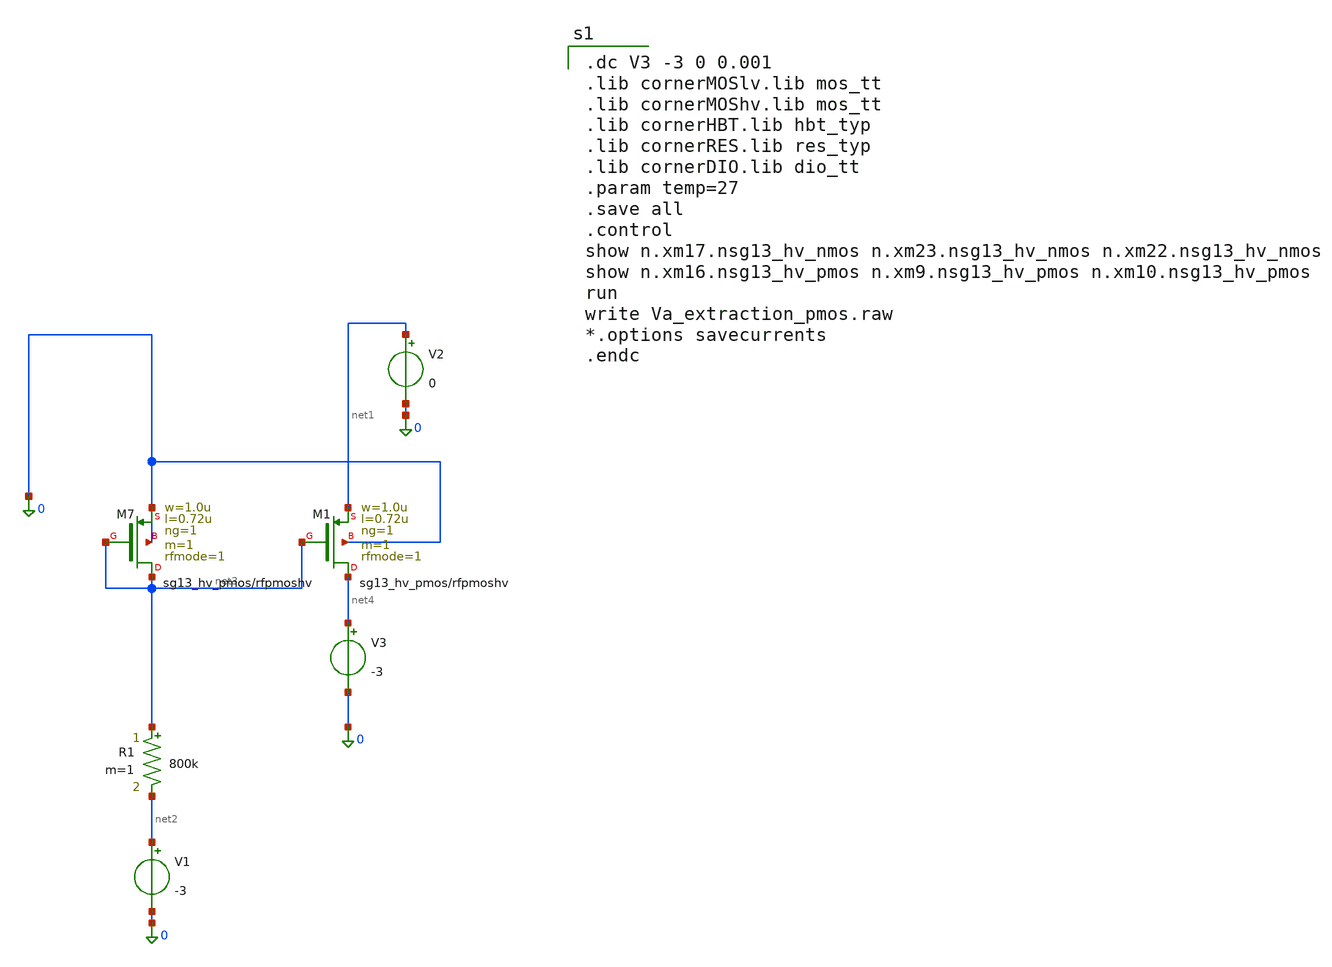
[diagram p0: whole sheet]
** sch_path: src/Va_extraction_pmos.sch
**.subckt Va_extraction_pmos
R1 net3 net2 800k m=1
XM7 net3 net3 0 0 sg13_hv_pmos w=1.0u l=0.72u ng=1 m=1 rfmode=1 mm_ok=1
XM1 net4 net3 net1 0 sg13_hv_pmos w=1.0u l=0.72u ng=1 m=1 rfmode=1 mm_ok=1
V3 net4 0 -3
V1 net2 0 -3
V2 net1 0 0
**** begin user architecture code

.dc V3 -3 0 0.001
.lib cornerMOSlv.lib mos_tt
.lib cornerMOShv.lib mos_tt
.lib cornerHBT.lib hbt_typ
.lib cornerRES.lib res_typ
.lib cornerDIO.lib dio_tt
.param temp=27
.save all
.control
show n.xm17.nsg13_hv_nmos n.xm23.nsg13_hv_nmos n.xm22.nsg13_hv_nmos
show n.xm16.nsg13_hv_pmos n.xm9.nsg13_hv_pmos n.xm10.nsg13_hv_pmos
run
write Va_extraction_pmos.raw
*.options savecurrents
.endc

**** end user architecture code
**.ends
.end
